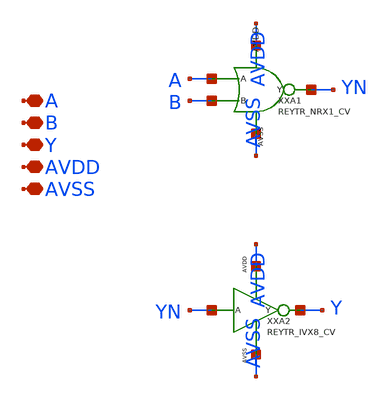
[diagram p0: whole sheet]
** sch_path: design/REY_TR_SKY130A/REYTR_ORX8_CV.sch
**.subckt REYTR_ORX8_CV A B Y AVDD AVSS
*.iopin A
*.iopin B
*.iopin Y
*.iopin AVDD
*.iopin AVSS
XXA1 A B YN AVDD AVSS REYTR_NRX1_CV
XXA2 AVSS AVDD YN Y REYTR_IVX8_CV
**.ends
.end
